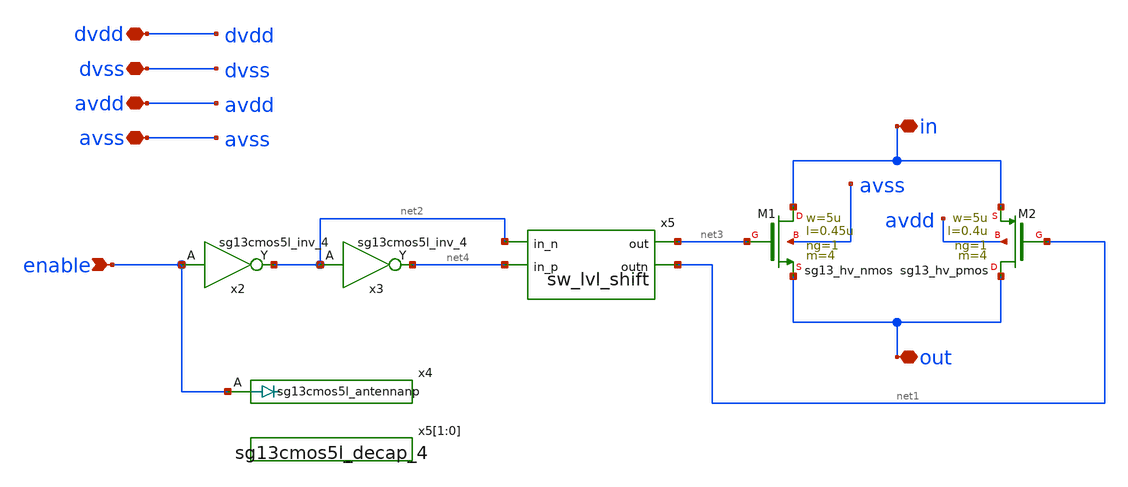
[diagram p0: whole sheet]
** sch_path: macros/ocd_analog_switches/schematic/xschem/analog_switch_small.sch
**.subckt analog_switch_small in out enable dvdd dvss avdd avss
*.iopin in
*.iopin out
*.ipin enable
*.iopin dvdd
*.iopin dvss
*.iopin avdd
*.iopin avss
XM1 in net3 out avss sg13_hv_nmos w=5u l=0.45u ng=1 m=4 mm_ok=1
XM2 out net1 in avdd sg13_hv_pmos w=5u l=0.4u ng=1 m=4 mm_ok=1
x2 net2 enable dvdd dvss sg13cmos5l_inv_4
x3 net4 net2 dvdd dvss sg13cmos5l_inv_4
x4 enable dvdd dvss sg13cmos5l_antennanp
x5[1] dvdd dvss sg13cmos5l_decap_4
x5[0] dvdd dvss sg13cmos5l_decap_4
x5 net4 net2 net3 net1 avdd avss sw_lvl_shift
**.ends

* expanding   symbol:  sw_lvl_shift.sym # of pins=4
** sym_path: macros/ocd_analog_switches/schematic/xschem/sw_lvl_shift.sym
** sch_path: macros/ocd_analog_switches/schematic/xschem/sw_lvl_shift.sch
.subckt sw_lvl_shift in_p in_n out outn avdd avss
*.ipin in_n
*.ipin in_p
*.opin out
*.opin outn
XM1 net1 in_p avss avss sg13_hv_nmos w=2u l=0.5u ng=1 m=1 mm_ok=1
XM2 net1 S1_N avdd avdd sg13_hv_pmos w=0.5u l=0.5u ng=1 m=1 mm_ok=1
XM3 S1_N in_n avss avss sg13_hv_nmos w=2u l=0.5u ng=1 m=1 mm_ok=1
XM4 S1_N net1 avdd avdd sg13_hv_pmos w=0.5u l=0.5u ng=1 m=1 mm_ok=1
XM5 outn S1_N avdd avdd sg13_hv_pmos w=2u l=0.5u ng=1 m=2 mm_ok=1
XM6 outn S1_N avss avss sg13_hv_nmos w=1u l=0.5u ng=1 m=2 mm_ok=1
XM7 out outn avdd avdd sg13_hv_pmos w=2u l=0.5u ng=1 m=2 mm_ok=1
XM8 out outn avss avss sg13_hv_nmos w=1u l=0.5u ng=1 m=2 mm_ok=1
.ends

.end
